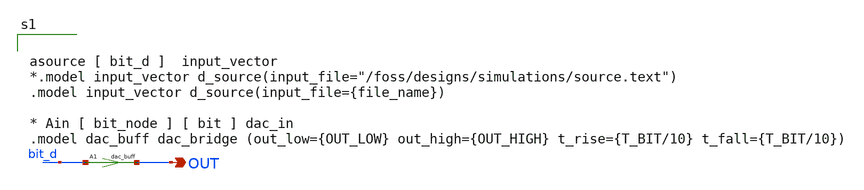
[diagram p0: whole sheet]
** sch_path: designs/libs/sim_support/vbit_file_trial.sch
**.subckt vbit_file_trial OUT
*.opin OUT
A1 [ bit_d ] [ OUT ] dac_buff
**** begin user architecture code


asource [ bit_d ]  input_vector
*.model input_vector d_source(input_file="/foss/designs/simulations/source.text")
.model input_vector d_source(input_file={file_name})

* Ain [ bit_node ] [ bit ] dac_in
.model dac_buff dac_bridge (out_low={OUT_LOW} out_high={OUT_HIGH} t_rise={T_BIT/10} t_fall={T_BIT/10})

**** end user architecture code
**.ends
.end
